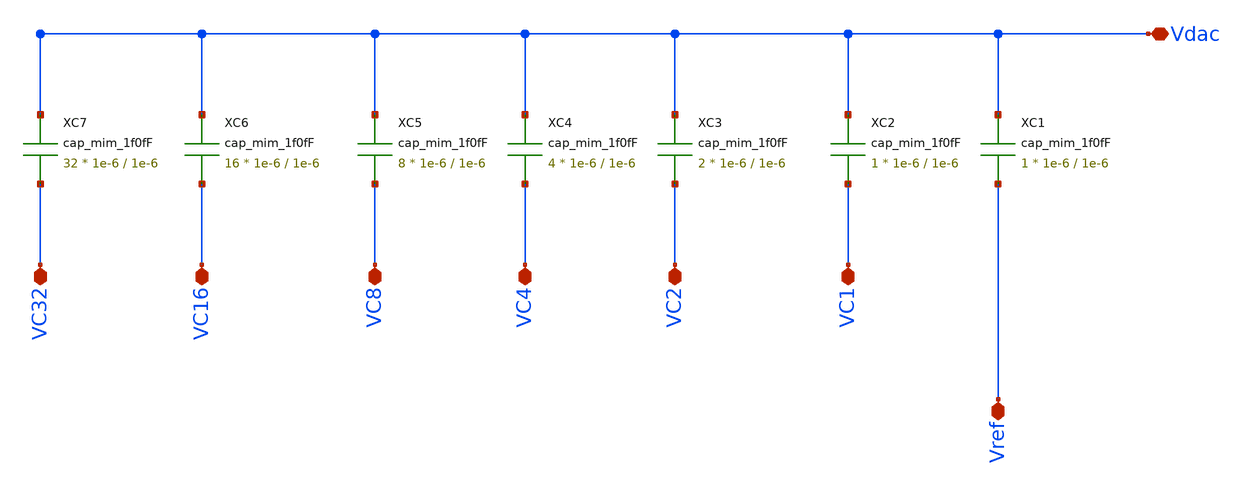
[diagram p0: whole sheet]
** sch_path: designs/libs/wk_kadam/c_dav_v1.sch
**.subckt c_dav_v1 Vref VC1 VC2 VC4 VC8 VC16 VC32 Vdac
*.iopin Vref
*.iopin VC1
*.iopin VC2
*.iopin VC4
*.iopin VC8
*.iopin VC16
*.iopin VC32
*.iopin Vdac
XC1 Vdac Vref cap_mim_1f0fF c_width=1e-6 c_length=1e-6 m=1
XC2 Vdac VC1 cap_mim_1f0fF c_width=1e-6 c_length=1e-6 m=1
XC3 Vdac VC2 cap_mim_1f0fF c_width=1e-6 c_length=1e-6 m=2
XC4 Vdac VC4 cap_mim_1f0fF c_width=1e-6 c_length=1e-6 m=4
XC5 Vdac VC8 cap_mim_1f0fF c_width=1e-6 c_length=1e-6 m=8
XC6 Vdac VC16 cap_mim_1f0fF c_width=1e-6 c_length=1e-6 m=16
XC7 Vdac VC32 cap_mim_1f0fF c_width=1e-6 c_length=1e-6 m=32
**.ends
.end
